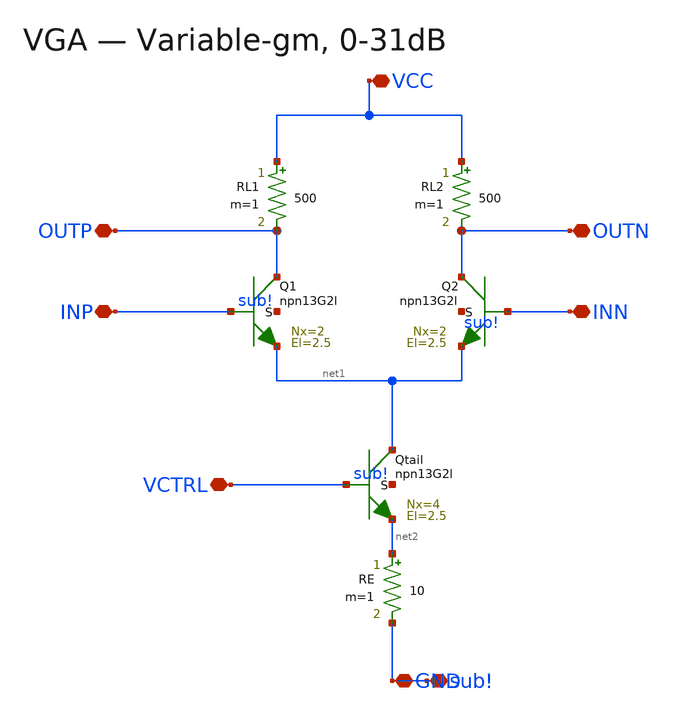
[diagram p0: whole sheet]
** sch_path: xschem/blocks/VGA_77G.sch
**.subckt VGA_77G INP INN OUTP OUTN VCTRL VCC GND sub!
*.iopin INP
*.iopin INN
*.iopin OUTP
*.iopin OUTN
*.iopin VCTRL
*.iopin VCC
*.iopin GND
*.iopin sub!
XQ1 OUTP INP net1 sub! npn13G2l Nx=2 El=2.5 mm_ok=1
XQ2 OUTN INN net1 sub! npn13G2l Nx=2 El=2.5 mm_ok=1
XQtail net1 VCTRL net2 sub! npn13G2l Nx=4 El=2.5 mm_ok=1
RL1 VCC OUTP 500 m=1
RL2 VCC OUTN 500 m=1
RE net2 GND 10 m=1
**.ends
.end
